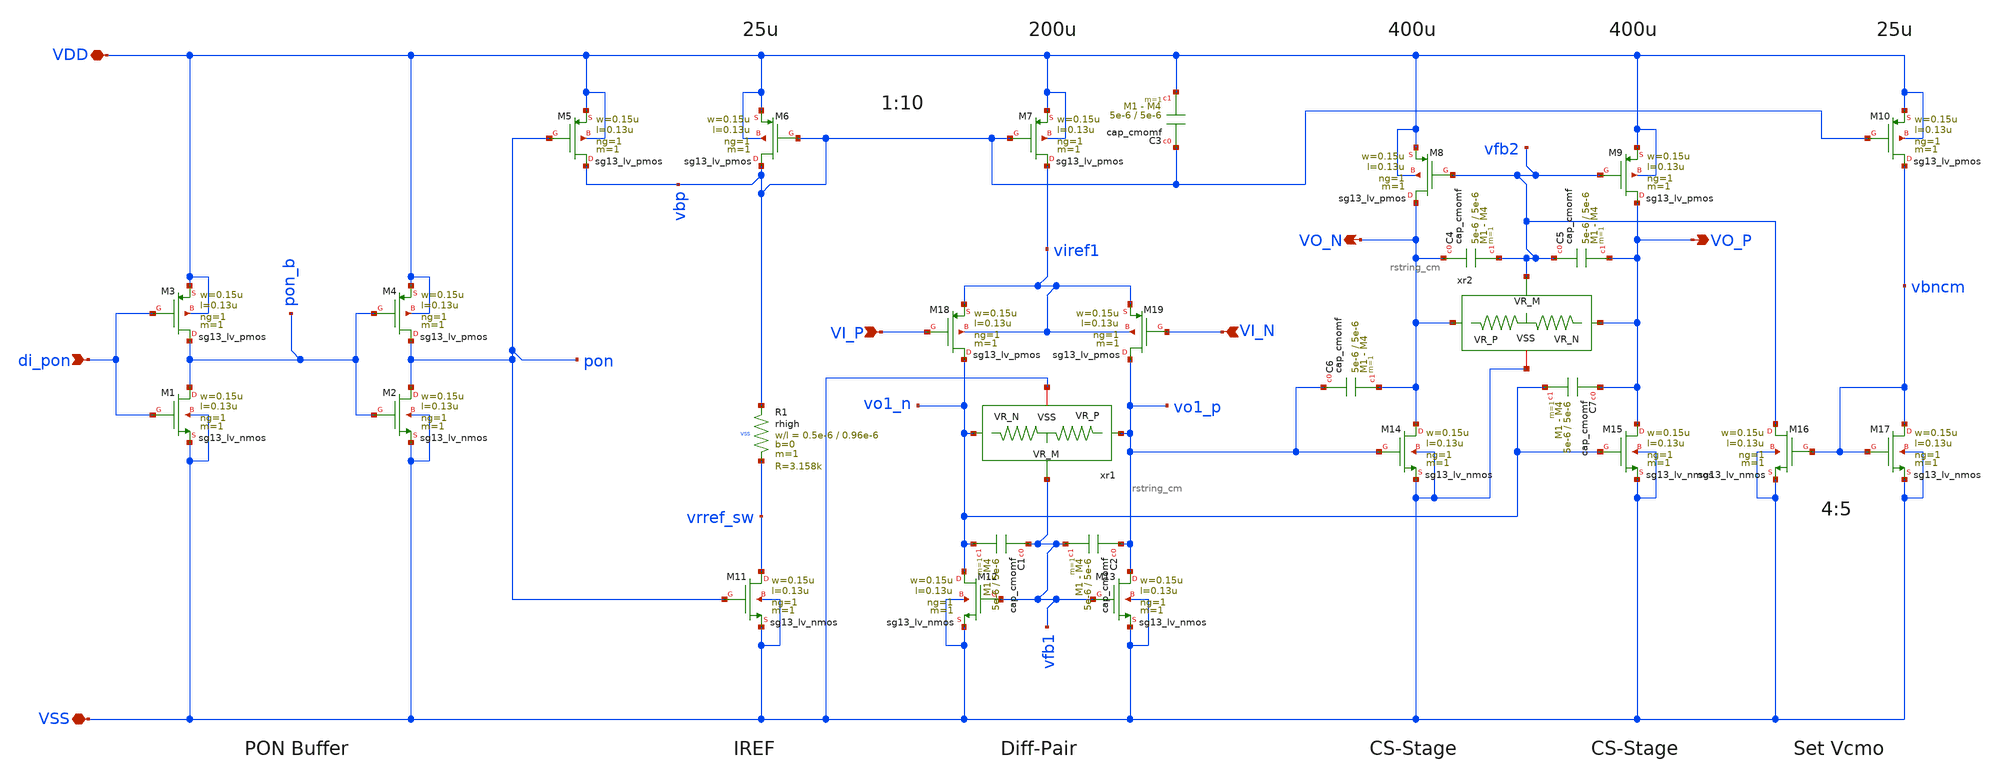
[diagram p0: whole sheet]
** sch_path: macros/filter_cmos5l/schematic/xschem/amp_bak0.sch
**.subckt amp_bak0 VSS VDD VI_P di_pon VI_N VO_P VO_N
*.iopin VSS
*.iopin VDD
*.ipin VI_P
*.ipin di_pon
*.ipin VI_N
*.opin VO_P
*.opin VO_N
xr1 vfb1 vo1_n vo1_p VSS rstring_cm
xr2 vfb2 VO_P VO_N VSS rstring_cm
XM1 pon_b di_pon VSS VSS sg13_lv_nmos w=0.15u l=0.13u ng=1 m=1 mm_ok=1
XM2 pon pon_b VSS VSS sg13_lv_nmos w=0.15u l=0.13u ng=1 m=1 mm_ok=1
XM3 pon_b di_pon VDD VDD sg13_lv_pmos w=0.15u l=0.13u ng=1 m=1 mm_ok=1
XM4 pon pon_b VDD VDD sg13_lv_pmos w=0.15u l=0.13u ng=1 m=1 mm_ok=1
XM5 vbp pon VDD VDD sg13_lv_pmos w=0.15u l=0.13u ng=1 m=1 mm_ok=1
XM6 vbp vbp VDD VDD sg13_lv_pmos w=0.15u l=0.13u ng=1 m=1 mm_ok=1
XM7 viref1 vbp VDD VDD sg13_lv_pmos w=0.15u l=0.13u ng=1 m=1 mm_ok=1
XM8 VO_N vfb2 VDD VDD sg13_lv_pmos w=0.15u l=0.13u ng=1 m=1 mm_ok=1
XM9 VO_P vfb2 VDD VDD sg13_lv_pmos w=0.15u l=0.13u ng=1 m=1 mm_ok=1
XM10 vbncm vbp VDD VDD sg13_lv_pmos w=0.15u l=0.13u ng=1 m=1 mm_ok=1
XM11 vrref_sw pon VSS VSS sg13_lv_nmos w=0.15u l=0.13u ng=1 m=1 mm_ok=1
XM12 vo1_n vfb1 VSS VSS sg13_lv_nmos w=0.15u l=0.13u ng=1 m=1 mm_ok=1
XM13 vo1_p vfb1 VSS VSS sg13_lv_nmos w=0.15u l=0.13u ng=1 m=1 mm_ok=1
XM14 VO_N vo1_p VSS VSS sg13_lv_nmos w=0.15u l=0.13u ng=1 m=1 mm_ok=1
XM15 VO_P vo1_n VSS VSS sg13_lv_nmos w=0.15u l=0.13u ng=1 m=1 mm_ok=1
XM16 vfb2 vbncm VSS VSS sg13_lv_nmos w=0.15u l=0.13u ng=1 m=1 mm_ok=1
XM17 vbncm vbncm VSS VSS sg13_lv_nmos w=0.15u l=0.13u ng=1 m=1 mm_ok=1
XM18 vo1_n VI_P viref1 viref1 sg13_lv_pmos w=0.15u l=0.13u ng=1 m=1 mm_ok=1
XM19 vo1_p VI_N viref1 viref1 sg13_lv_pmos w=0.15u l=0.13u ng=1 m=1 mm_ok=1
XR1 vbp vrref_sw VSS rhigh w=0.5e-6 l=0.96e-6 m=1 b=0 mm_ok=1
XC1 vfb1 vo1_n cap_cmomf w=5e-6 l=5e-6 mmin=1 mmax=4 subblock=0 rfmodel=0 subscale=1 m=1 mm_ok=1
XC2 vo1_p vfb1 cap_cmomf w=5e-6 l=5e-6 mmin=1 mmax=4 subblock=0 rfmodel=0 subscale=1 m=1 mm_ok=1
XC3 vbp VDD cap_cmomf w=5e-6 l=5e-6 mmin=1 mmax=4 subblock=0 rfmodel=0 subscale=1 m=1 mm_ok=1
XC4 VO_N vfb2 cap_cmomf w=5e-6 l=5e-6 mmin=1 mmax=4 subblock=0 rfmodel=0 subscale=1 m=1 mm_ok=1
XC5 vfb2 VO_P cap_cmomf w=5e-6 l=5e-6 mmin=1 mmax=4 subblock=0 rfmodel=0 subscale=1 m=1 mm_ok=1
XC6 vo1_p VO_N cap_cmomf w=5e-6 l=5e-6 mmin=1 mmax=4 subblock=0 rfmodel=0 subscale=1 m=1 mm_ok=1
XC7 VO_P vo1_n cap_cmomf w=5e-6 l=5e-6 mmin=1 mmax=4 subblock=0 rfmodel=0 subscale=1 m=1 mm_ok=1
**.ends

* expanding   symbol:  rstring_cm.sym # of pins=4
** sym_path: rstring_cm.sym
** sch_path: rstring_cm.sch
.subckt rstring_cm VR_M VR_N VR_P VSS
*.iopin VSS
*.ipin VR_P
*.ipin VR_N
*.opin VR_M
XR1 VR_P net1 VSS rhigh w=0.5e-6 l=0.96e-6 m=1 b=0 mm_ok=1
XR2 net1 VR_M VSS rhigh w=0.5e-6 l=0.96e-6 m=1 b=0 mm_ok=1
XR3 VR_M net2 VSS rhigh w=0.5e-6 l=0.96e-6 m=1 b=0 mm_ok=1
XR4 net2 VR_N VSS rhigh w=0.5e-6 l=0.96e-6 m=1 b=0 mm_ok=1
.ends

.end
